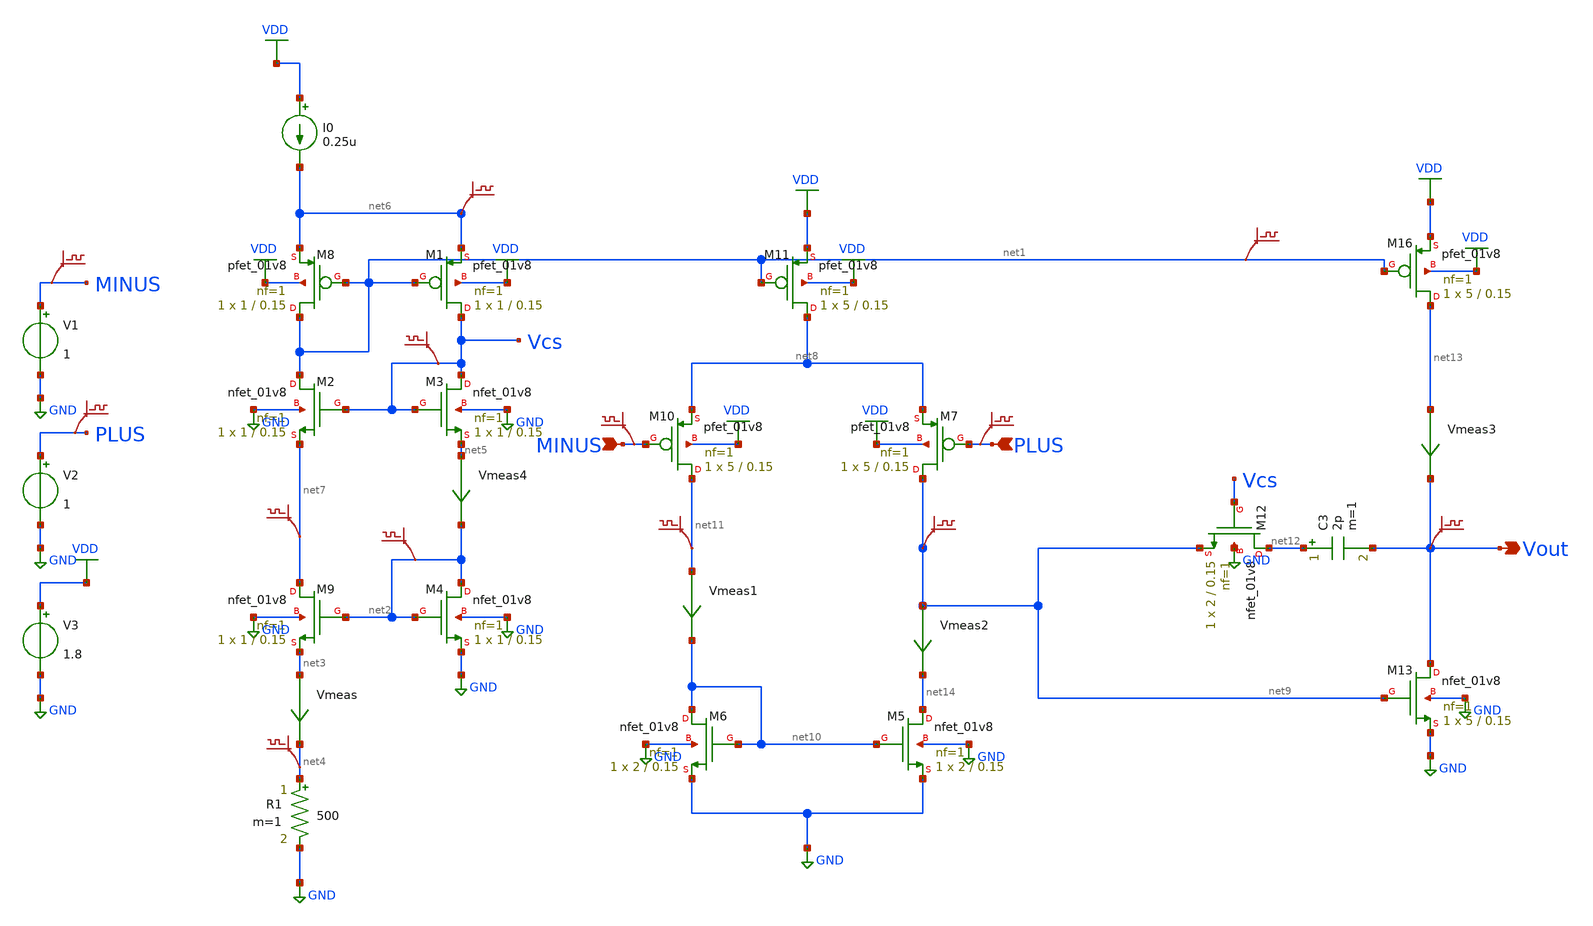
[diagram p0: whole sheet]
** sch_path: lib/xschem/LDO/opamp_2stage.sch
**.subckt opamp_2stage PLUS MINUS Vout
*.ipin PLUS
*.ipin MINUS
*.opin Vout
XM8 net1 net1 net6 VDD sky130_fd_pr__pfet_01v8 L=0.15 W=1 nf=1 ad='int((nf+1)/2) * W/nf * 0.29' as='int((nf+2)/2) * W/nf * 0.29'
+ pd='2*int((nf+1)/2) * (W/nf + 0.29)' ps='2*int((nf+2)/2) * (W/nf + 0.29)' nrd='0.29 / W' nrs='0.29 / W'
+ sa=0 sb=0 sd=0 mult=1 m=1
XM9 net7 net2 net3 GND sky130_fd_pr__nfet_01v8 L=0.15 W=1 nf=1 ad='int((nf+1)/2) * W/nf * 0.29' as='int((nf+2)/2) * W/nf * 0.29'
+ pd='2*int((nf+1)/2) * (W/nf + 0.29)' ps='2*int((nf+2)/2) * (W/nf + 0.29)' nrd='0.29 / W' nrs='0.29 / W'
+ sa=0 sb=0 sd=0 mult=1 m=1
XM1 Vcs net1 net6 VDD sky130_fd_pr__pfet_01v8 L=0.15 W=1 nf=1 ad='int((nf+1)/2) * W/nf * 0.29' as='int((nf+2)/2) * W/nf * 0.29'
+ pd='2*int((nf+1)/2) * (W/nf + 0.29)' ps='2*int((nf+2)/2) * (W/nf + 0.29)' nrd='0.29 / W' nrs='0.29 / W'
+ sa=0 sb=0 sd=0 mult=1 m=1
XM2 net1 Vcs net7 GND sky130_fd_pr__nfet_01v8 L=0.15 W=1 nf=1 ad='int((nf+1)/2) * W/nf * 0.29' as='int((nf+2)/2) * W/nf * 0.29'
+ pd='2*int((nf+1)/2) * (W/nf + 0.29)' ps='2*int((nf+2)/2) * (W/nf + 0.29)' nrd='0.29 / W' nrs='0.29 / W'
+ sa=0 sb=0 sd=0 mult=1 m=1
XM3 Vcs Vcs net5 GND sky130_fd_pr__nfet_01v8 L=0.15 W=1 nf=1 ad='int((nf+1)/2) * W/nf * 0.29' as='int((nf+2)/2) * W/nf * 0.29'
+ pd='2*int((nf+1)/2) * (W/nf + 0.29)' ps='2*int((nf+2)/2) * (W/nf + 0.29)' nrd='0.29 / W' nrs='0.29 / W'
+ sa=0 sb=0 sd=0 mult=1 m=1
XM4 net2 net2 GND GND sky130_fd_pr__nfet_01v8 L=0.15 W=1 nf=1 ad='int((nf+1)/2) * W/nf * 0.29' as='int((nf+2)/2) * W/nf * 0.29'
+ pd='2*int((nf+1)/2) * (W/nf + 0.29)' ps='2*int((nf+2)/2) * (W/nf + 0.29)' nrd='0.29 / W' nrs='0.29 / W'
+ sa=0 sb=0 sd=0 mult=1 m=1
R1 net4 GND 500 m=1
C3 net12 Vout 2p m=1
XM6 net10 net10 GND GND sky130_fd_pr__nfet_01v8 L=0.15 W=2 nf=1 ad='int((nf+1)/2) * W/nf * 0.29' as='int((nf+2)/2) * W/nf * 0.29'
+ pd='2*int((nf+1)/2) * (W/nf + 0.29)' ps='2*int((nf+2)/2) * (W/nf + 0.29)' nrd='0.29 / W' nrs='0.29 / W'
+ sa=0 sb=0 sd=0 mult=1 m=1
XM5 net14 net10 GND GND sky130_fd_pr__nfet_01v8 L=0.15 W=2 nf=1 ad='int((nf+1)/2) * W/nf * 0.29' as='int((nf+2)/2) * W/nf * 0.29'
+ pd='2*int((nf+1)/2) * (W/nf + 0.29)' ps='2*int((nf+2)/2) * (W/nf + 0.29)' nrd='0.29 / W' nrs='0.29 / W'
+ sa=0 sb=0 sd=0 mult=1 m=1
XM7 net9 PLUS net8 VDD sky130_fd_pr__pfet_01v8 L=0.15 W=5 nf=1 ad='int((nf+1)/2) * W/nf * 0.29' as='int((nf+2)/2) * W/nf * 0.29'
+ pd='2*int((nf+1)/2) * (W/nf + 0.29)' ps='2*int((nf+2)/2) * (W/nf + 0.29)' nrd='0.29 / W' nrs='0.29 / W'
+ sa=0 sb=0 sd=0 mult=1 m=1
XM10 net11 MINUS net8 VDD sky130_fd_pr__pfet_01v8 L=0.15 W=5 nf=1 ad='int((nf+1)/2) * W/nf * 0.29' as='int((nf+2)/2) * W/nf * 0.29'
+ pd='2*int((nf+1)/2) * (W/nf + 0.29)' ps='2*int((nf+2)/2) * (W/nf + 0.29)' nrd='0.29 / W' nrs='0.29 / W'
+ sa=0 sb=0 sd=0 mult=1 m=1
XM11 net8 net1 VDD VDD sky130_fd_pr__pfet_01v8 L=0.15 W=5 nf=1 ad='int((nf+1)/2) * W/nf * 0.29' as='int((nf+2)/2) * W/nf * 0.29'
+ pd='2*int((nf+1)/2) * (W/nf + 0.29)' ps='2*int((nf+2)/2) * (W/nf + 0.29)' nrd='0.29 / W' nrs='0.29 / W'
+ sa=0 sb=0 sd=0 mult=1 m=1
XM13 Vout net9 GND GND sky130_fd_pr__nfet_01v8 L=0.15 W=5 nf=1 ad='int((nf+1)/2) * W/nf * 0.29' as='int((nf+2)/2) * W/nf * 0.29'
+ pd='2*int((nf+1)/2) * (W/nf + 0.29)' ps='2*int((nf+2)/2) * (W/nf + 0.29)' nrd='0.29 / W' nrs='0.29 / W'
+ sa=0 sb=0 sd=0 mult=1 m=1
XM16 net13 net1 VDD VDD sky130_fd_pr__pfet_01v8 L=0.15 W=5 nf=1 ad='int((nf+1)/2) * W/nf * 0.29' as='int((nf+2)/2) * W/nf * 0.29'
+ pd='2*int((nf+1)/2) * (W/nf + 0.29)' ps='2*int((nf+2)/2) * (W/nf + 0.29)' nrd='0.29 / W' nrs='0.29 / W'
+ sa=0 sb=0 sd=0 mult=1 m=1
V2 PLUS GND 1
V3 VDD GND 1.8
V1 MINUS GND 1
.save v(plus)
.save v(minus)
.save v(net1)
.save v(net9)
.save v(net11)
Vmeas net3 net4 0
.save i(vmeas)
.save v(minus)
.save v(vout)
.save v(plus)
.save v(net6)
.save v(net4)
Vmeas1 net11 net10 0
.save i(vmeas1)
Vmeas2 net9 net14 0
.save i(vmeas2)
Vmeas3 net13 Vout 0
.save i(vmeas3)
Vmeas4 net5 net2 0
.save i(vmeas4)
.save v(net2)
.save v(net7)
.save v(vcs)
XM12 net12 Vcs net9 GND sky130_fd_pr__nfet_01v8 L=0.15 W=2 nf=1 ad='int((nf+1)/2) * W/nf * 0.29' as='int((nf+2)/2) * W/nf * 0.29'
+ pd='2*int((nf+1)/2) * (W/nf + 0.29)' ps='2*int((nf+2)/2) * (W/nf + 0.29)' nrd='0.29 / W' nrs='0.29 / W'
+ sa=0 sb=0 sd=0 mult=1 m=1
I0 VDD net6 0.25u
**** begin user architecture code

.lib $::SKYWATER_MODELS/sky130.lib.spice tt


**** end user architecture code
**.ends
.GLOBAL VDD
.GLOBAL GND
**** begin user architecture code



.control
save all
op
write opamp_2stage.raw
.endc


**** end user architecture code
.end
